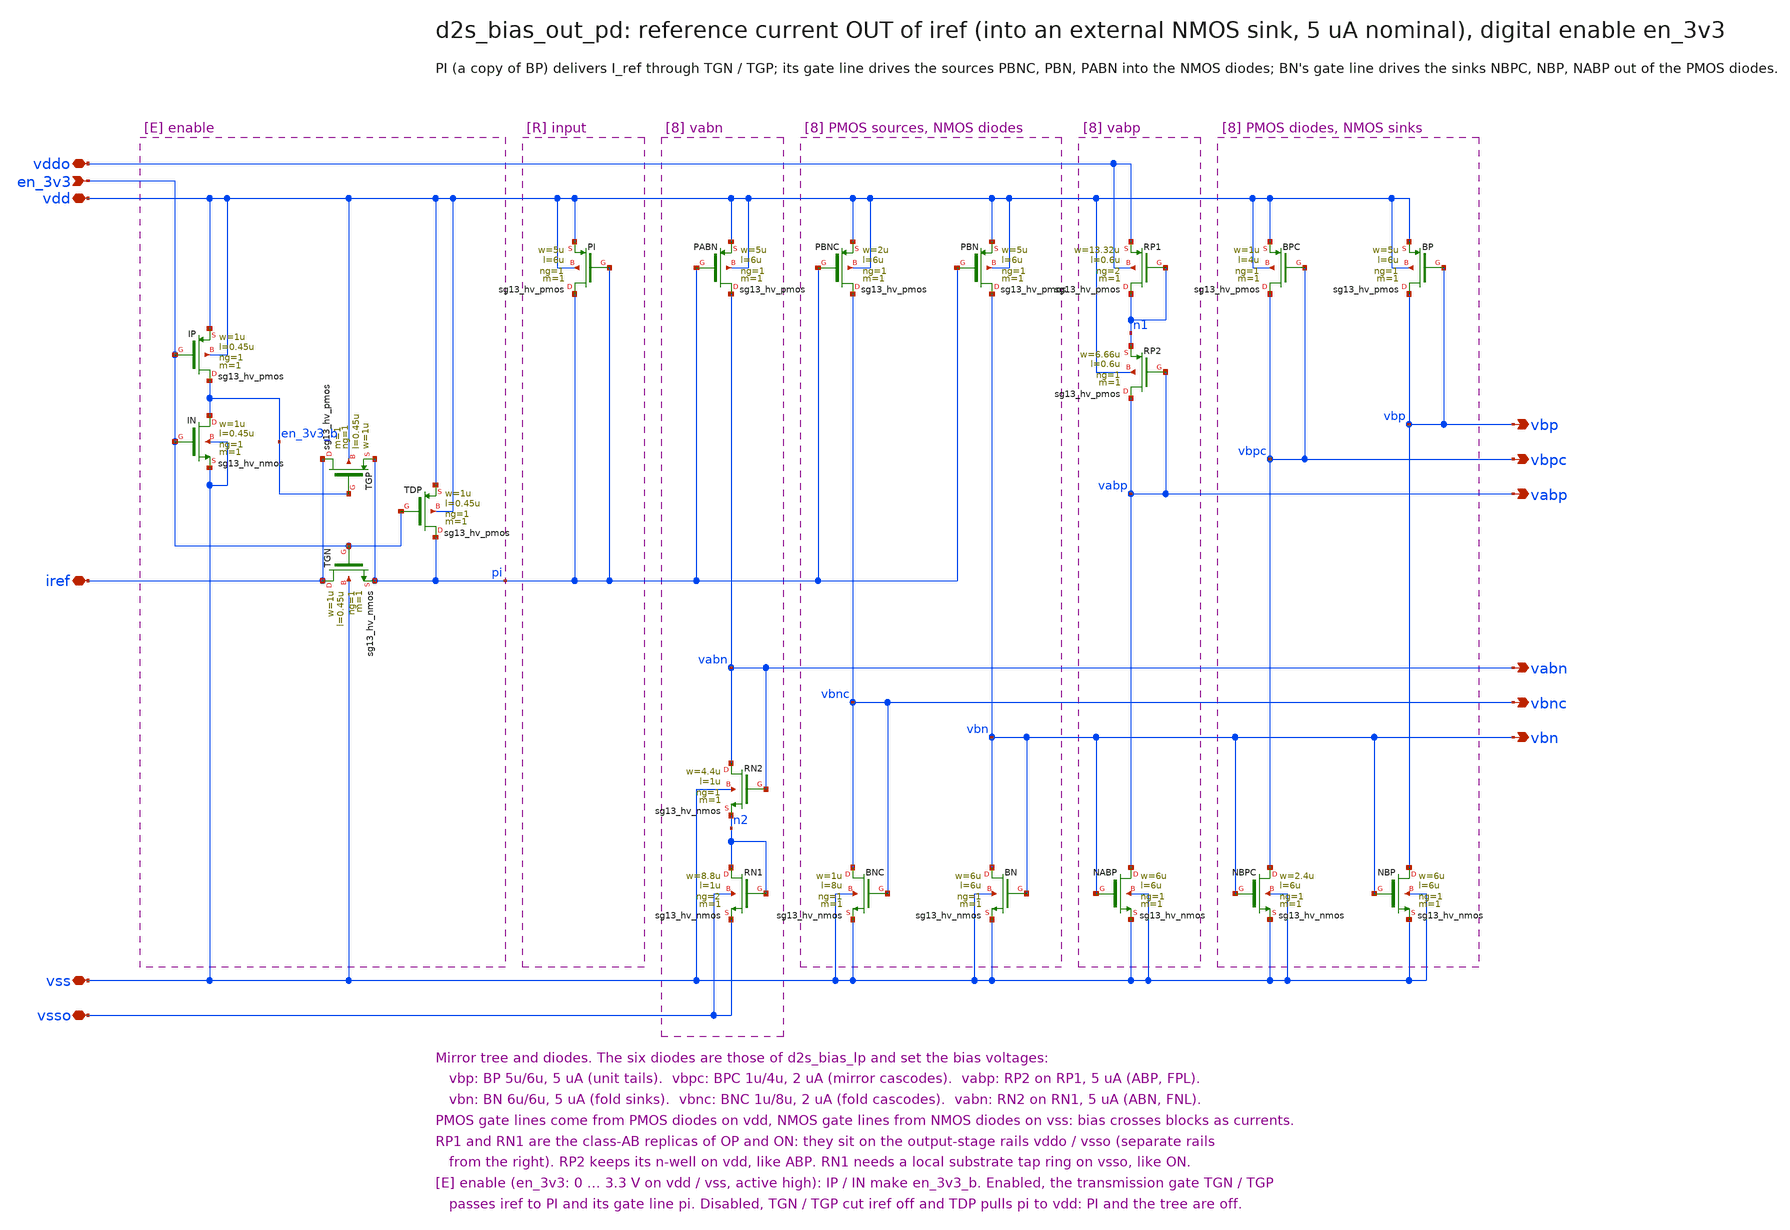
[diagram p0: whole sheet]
** sch_path: sudelbuecher/design_considerations/class_ab_pad_driver/power_down/xschem/d2s_bias_out_pd.sch
**.subckt d2s_bias_out_pd vdd vss vddo vsso iref vbp vbn vbpc vbnc vabp vabn en_3v3
*.iopin vdd
*.iopin vss
*.iopin vddo
*.iopin vsso
*.iopin iref
*.opin vbp
*.opin vbn
*.opin vbpc
*.opin vbnc
*.opin vabp
*.opin vabn
*.ipin en_3v3
XPI pi pi vdd vdd sg13_hv_pmos w=5u l=6u ng=1 m=1 mm_ok=1
XBPC vbpc vbpc vdd vdd sg13_hv_pmos w=1u l=4u ng=1 m=1 mm_ok=1
XNBPC vbpc vbn vss vss sg13_hv_nmos w=2.4u l=6u ng=1 m=1 mm_ok=1
XBP vbp vbp vdd vdd sg13_hv_pmos w=5u l=6u ng=1 m=1 mm_ok=1
XNBP vbp vbn vss vss sg13_hv_nmos w=6u l=6u ng=1 m=1 mm_ok=1
XRP1 n1 n1 vddo vddo sg13_hv_pmos w=13.32u l=0.6u ng=2 m=1 mm_ok=1
XRP2 vabp vabp n1 vdd sg13_hv_pmos w=6.66u l=0.6u ng=1 m=1 mm_ok=1
XNABP vabp vbn vss vss sg13_hv_nmos w=6u l=6u ng=1 m=1 mm_ok=1
XPBNC vbnc pi vdd vdd sg13_hv_pmos w=2u l=6u ng=1 m=1 mm_ok=1
XBNC vbnc vbnc vss vss sg13_hv_nmos w=1u l=8u ng=1 m=1 mm_ok=1
XPBN vbn pi vdd vdd sg13_hv_pmos w=5u l=6u ng=1 m=1 mm_ok=1
XBN vbn vbn vss vss sg13_hv_nmos w=6u l=6u ng=1 m=1 mm_ok=1
XPABN vabn pi vdd vdd sg13_hv_pmos w=5u l=6u ng=1 m=1 mm_ok=1
XRN2 vabn vabn n2 vss sg13_hv_nmos w=4.4u l=1u ng=1 m=1 mm_ok=1
XRN1 n2 n2 vsso vsso sg13_hv_nmos w=8.8u l=1u ng=2 m=1 mm_ok=1
XIP en_3v3_b en_3v3 vdd vdd sg13_hv_pmos w=1u l=0.45u ng=1 m=1 mm_ok=1
XIN en_3v3_b en_3v3 vss vss sg13_hv_nmos w=1u l=0.45u ng=1 m=1 mm_ok=1
XTGP iref en_3v3_b pi vdd sg13_hv_pmos w=1u l=0.45u ng=1 m=1 mm_ok=1
XTGN iref en_3v3 pi vss sg13_hv_nmos w=1u l=0.45u ng=1 m=1 mm_ok=1
XTDP pi en_3v3 vdd vdd sg13_hv_pmos w=1u l=0.45u ng=1 m=1 mm_ok=1
**.ends
.end
